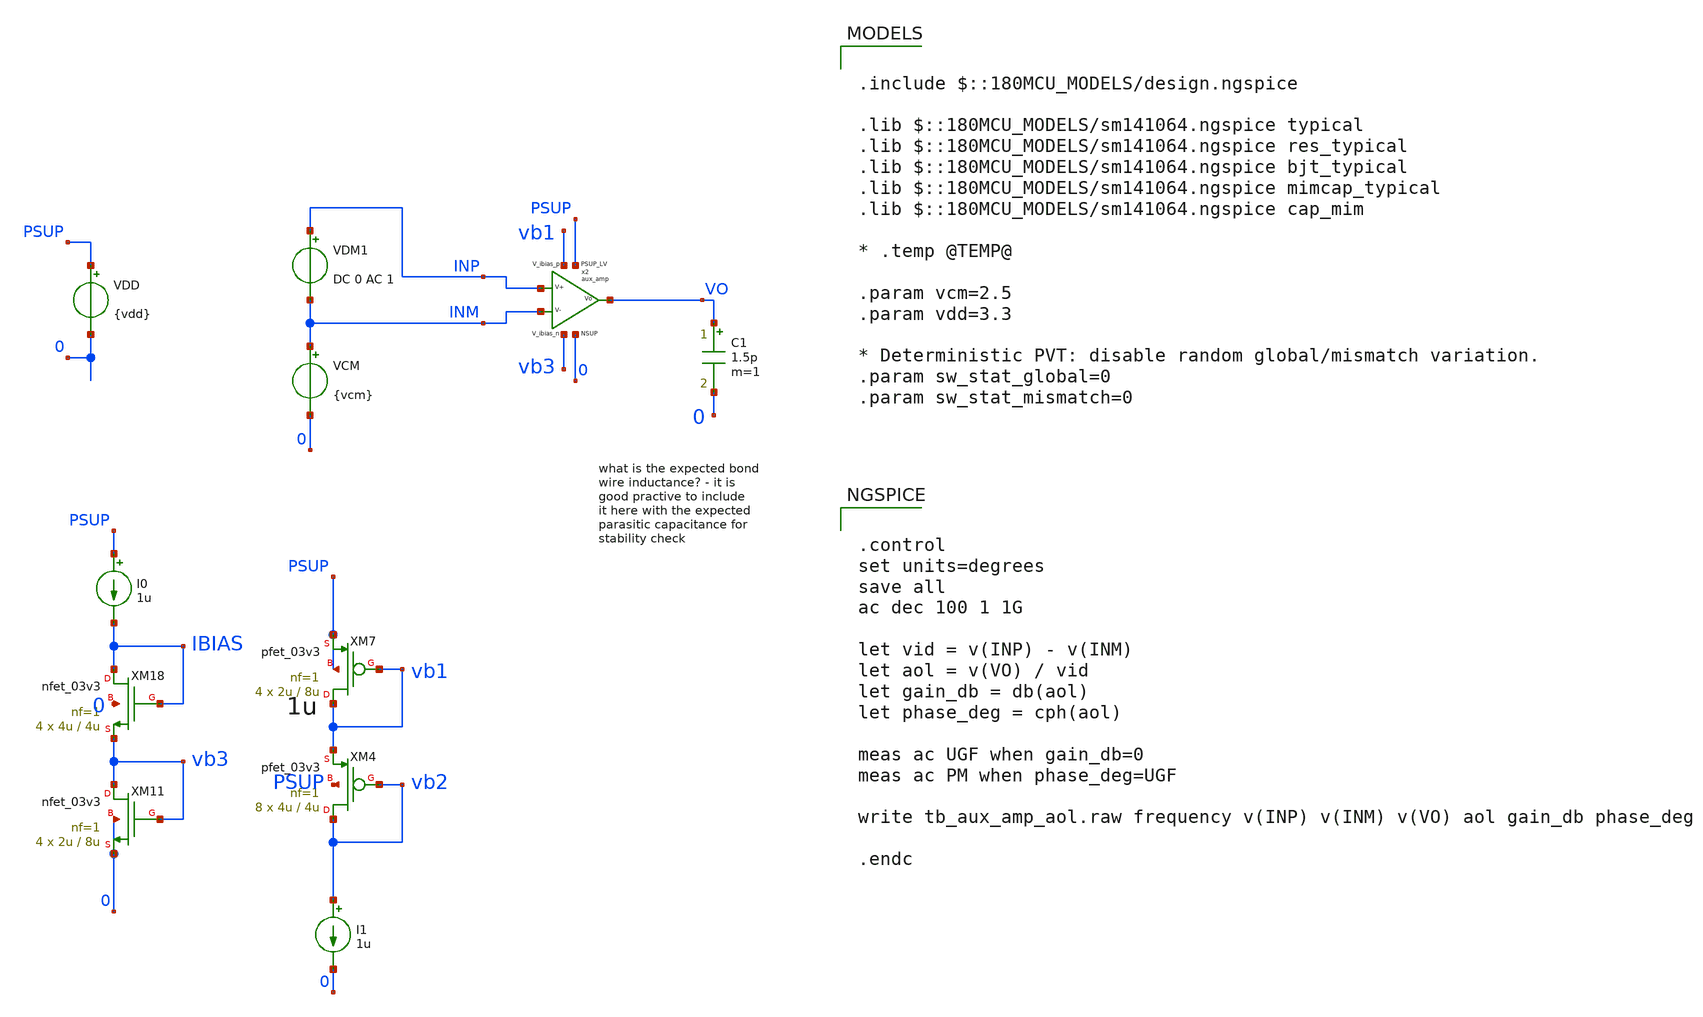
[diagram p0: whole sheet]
** sch_path: xschem/blocks/aux_amp/tb_aux_amp_aol.sch
**.subckt tb_aux_amp_aol
VDD PSUP 0 {vdd}
VCM INM 0 {vcm}
VDM1 INP INM DC 0 AC 1
C1 VO 0 1.5p m=1
XM11 vb3 vb3 0 0 nfet_03v3 L=8u W=2u nf=1 ad='int((nf+1)/2) * W/nf * 0.18u' as='int((nf+2)/2) * W/nf * 0.18u'
+ pd='2*int((nf+1)/2) * (W/nf + 0.18u)' ps='2*int((nf+2)/2) * (W/nf + 0.18u)' nrd='0.18u / W' nrs='0.18u / W'
+ sa=0 sb=0 sd=0 m=4
XM18 IBIAS IBIAS vb3 0 nfet_03v3 L=4u W=4u nf=1 ad='int((nf+1)/2) * W/nf * 0.18u' as='int((nf+2)/2) * W/nf * 0.18u'
+ pd='2*int((nf+1)/2) * (W/nf + 0.18u)' ps='2*int((nf+2)/2) * (W/nf + 0.18u)' nrd='0.18u / W' nrs='0.18u / W'
+ sa=0 sb=0 sd=0 m=4
I0 PSUP IBIAS 1u
XM7 vb1 vb1 PSUP PSUP pfet_03v3 L=8u W=2u nf=1 ad='int((nf+1)/2) * W/nf * 0.18u' as='int((nf+2)/2) * W/nf * 0.18u'
+ pd='2*int((nf+1)/2) * (W/nf + 0.18u)' ps='2*int((nf+2)/2) * (W/nf + 0.18u)' nrd='0.18u / W' nrs='0.18u / W'
+ sa=0 sb=0 sd=0 m=4
XM4 vb2 vb2 vb1 PSUP pfet_03v3 L=4u W=4u nf=1 ad='int((nf+1)/2) * W/nf * 0.18u' as='int((nf+2)/2) * W/nf * 0.18u'
+ pd='2*int((nf+1)/2) * (W/nf + 0.18u)' ps='2*int((nf+2)/2) * (W/nf + 0.18u)' nrd='0.18u / W' nrs='0.18u / W'
+ sa=0 sb=0 sd=0 m=8
I1 vb2 0 1u
x2 PSUP VO INP INM vb3 0 vb1 aux_amp
**** begin user architecture code

.include $::180MCU_MODELS/design.ngspice

.lib $::180MCU_MODELS/sm141064.ngspice typical
.lib $::180MCU_MODELS/sm141064.ngspice res_typical
.lib $::180MCU_MODELS/sm141064.ngspice bjt_typical
.lib $::180MCU_MODELS/sm141064.ngspice mimcap_typical
.lib $::180MCU_MODELS/sm141064.ngspice cap_mim

* .temp @TEMP@

.param vcm=2.5
.param vdd=3.3

* Deterministic PVT: disable random global/mismatch variation.
.param sw_stat_global=0
.param sw_stat_mismatch=0



.control
set units=degrees
save all
ac dec 100 1 1G

let vid = v(INP) - v(INM)
let aol = v(VO) / vid
let gain_db = db(aol)
let phase_deg = cph(aol)

meas ac UGF when gain_db=0
meas ac PM when phase_deg=UGF

write tb_aux_amp_aol.raw frequency v(INP) v(INM) v(VO) aol gain_db phase_deg

.endc


**** end user architecture code
**.ends
.end
